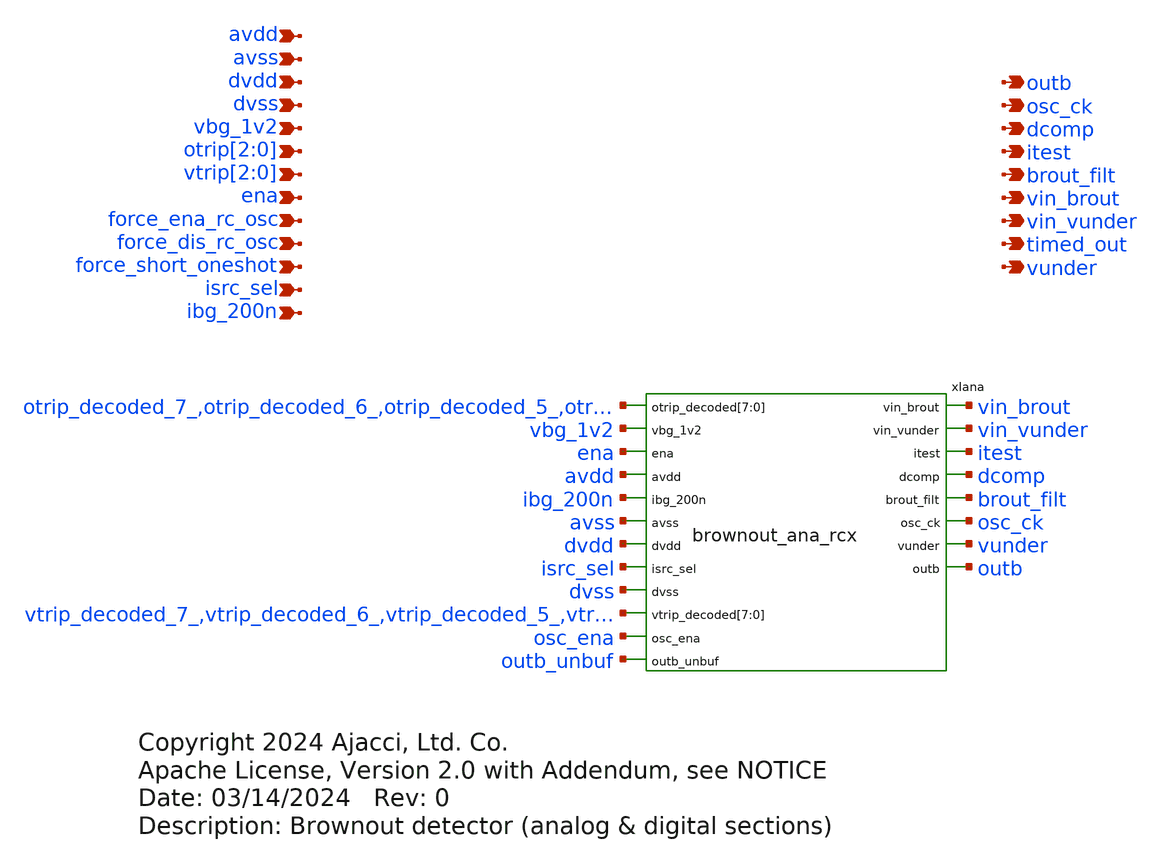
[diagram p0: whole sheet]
** sch_path: xschem/sky130_ajc_ip__brownout.sch
* Copyright 2024 Ajacci, Ltd. Co.
* Apache License, Version 2.0 with Addendum, see NOTICE
**.subckt sky130_ajc_ip__brownout avdd avss dvdd dvss vbg_1v2 otrip[2],otrip[1],otrip[0] ena
*+ force_dis_rc_osc force_short_oneshot isrc_sel ibg_200n vin_brout outb osc_ck brout_filt itest timed_out
*+ vtrip[2],vtrip[1],vtrip[0] vin_vunder vunder force_ena_rc_osc dcomp
*.ipin avdd
*.ipin avss
*.ipin dvdd
*.ipin dvss
*.ipin vbg_1v2
*.ipin otrip[2],otrip[1],otrip[0]
*.ipin ena
*.ipin force_dis_rc_osc
*.ipin force_short_oneshot
*.ipin isrc_sel
*.ipin ibg_200n
*.opin vin_brout
*.opin outb
*.opin osc_ck
*.opin brout_filt
*.opin itest
*.opin timed_out
*.ipin vtrip[2],vtrip[1],vtrip[0]
*.opin vin_vunder
*.opin vunder
*.ipin force_ena_rc_osc
*.opin dcomp
xIana vin_brout otrip_decoded_7_ otrip_decoded_6_ otrip_decoded_5_ otrip_decoded_4_ otrip_decoded_3_
+ otrip_decoded_2_ otrip_decoded_1_ otrip_decoded_0_ vin_vunder vbg_1v2 ena avdd ibg_200n itest avss dvdd isrc_sel
+ dvss vtrip_decoded_7_ vtrip_decoded_6_ vtrip_decoded_5_ vtrip_decoded_4_ vtrip_decoded_3_
+ vtrip_decoded_2_ vtrip_decoded_1_ vtrip_decoded_0_ dcomp brout_filt osc_ck osc_ena vunder outb outb_unbuf
+ brownout_ana_rcx
**** begin user architecture code



r0 otrip[0] otrip0 1
r1 otrip[1] otrip1 1
r2 otrip[2] otrip2 1
r3 vtrip[0] vtrip0 1
r4 vtrip[1] vtrip1 1
r5 vtrip[2] vtrip2 1

*XSPICE CO-SIM netlist
.include brownout_dig.out.spice
xibrownout_dig dvss dvdd brout_filt dcomp ena force_dis_rc_osc force_ena_rc_osc force_short_oneshot
+ osc_ck osc_ena  otrip0 otrip1 otrip2 otrip_decoded_0_ otrip_decoded_1_ otrip_decoded_2_ otrip_decoded_3_
+ otrip_decoded_4_ otrip_decoded_5_ otrip_decoded_6_ otrip_decoded_7_ outb_unbuf timed_out vtrip0 vtrip1 vtrip2
+ vtrip_decoded_0_ vtrip_decoded_1_ vtrip_decoded_2_ vtrip_decoded_3_ vtrip_decoded_4_ vtrip_decoded_5_
+ vtrip_decoded_6_ vtrip_decoded_7_ brownout_dig


**** end user architecture code
**.ends

* expanding   symbol:  xschem/brownout_ana_rcx.sym # of pins=20
** sym_path: xschem/brownout_ana_rcx.sym
** sch_path: xschem/brownout_ana_rcx.sch
.subckt brownout_ana_rcx vin_brout otrip_decoded[7] otrip_decoded[6] otrip_decoded[5]
+ otrip_decoded[4] otrip_decoded[3] otrip_decoded[2] otrip_decoded[1] otrip_decoded[0] vin_vunder vbg_1v2 ena avdd
+ ibg_200n itest avss dvdd isrc_sel dvss vtrip_decoded[7] vtrip_decoded[6] vtrip_decoded[5] vtrip_decoded[4]
+ vtrip_decoded[3] vtrip_decoded[2] vtrip_decoded[1] vtrip_decoded[0] dcomp brout_filt osc_ck osc_ena vunder outb
+ outb_unbuf
*.ipin vbg_1v2
*.ipin avdd
*.ipin avss
*.ipin dvdd
*.ipin dvss
*.ipin ena
*.ipin isrc_sel
*.ipin ibg_200n
*.opin dcomp
*.opin itest
*.ipin osc_ena
*.opin osc_ck
*.ipin
*+ otrip_decoded[7],otrip_decoded[6],otrip_decoded[5],otrip_decoded[4],otrip_decoded[3],otrip_decoded[2],otrip_decoded[1],otrip_decoded[0]
*.opin vin_brout
*.ipin outb_unbuf
*.opin outb
*.opin vunder
*.ipin
*+ vtrip_decoded[7],vtrip_decoded[6],vtrip_decoded[5],vtrip_decoded[4],vtrip_decoded[3],vtrip_decoded[2],vtrip_decoded[1],vtrip_decoded[0]
*.opin vin_vunder
*.opin brout_filt
**** begin user architecture code



.include mag/rcx/brownout_ana_rcx.spice

xIana vin_brout otrip_decoded[7] otrip_decoded[6] otrip_decoded[5] otrip_decoded[4] otrip_decoded[3]
+ otrip_decoded[2]  otrip_decoded[1] otrip_decoded[0] vin_vunder vbg_1v2 ena avdd ibg_200n itest avss dvdd isrc_sel
+ dvss vtrip_decoded[7] vtrip_decoded[6]  vtrip_decoded[5] vtrip_decoded[4] vtrip_decoded[3]
+ vtrip_decoded[2] vtrip_decoded[1] vtrip_decoded[0] dcomp brout_filt osc_ck osc_ena vunder outb  outb_unbuf
+ brownout_ana



**** end user architecture code
.ends

.end
